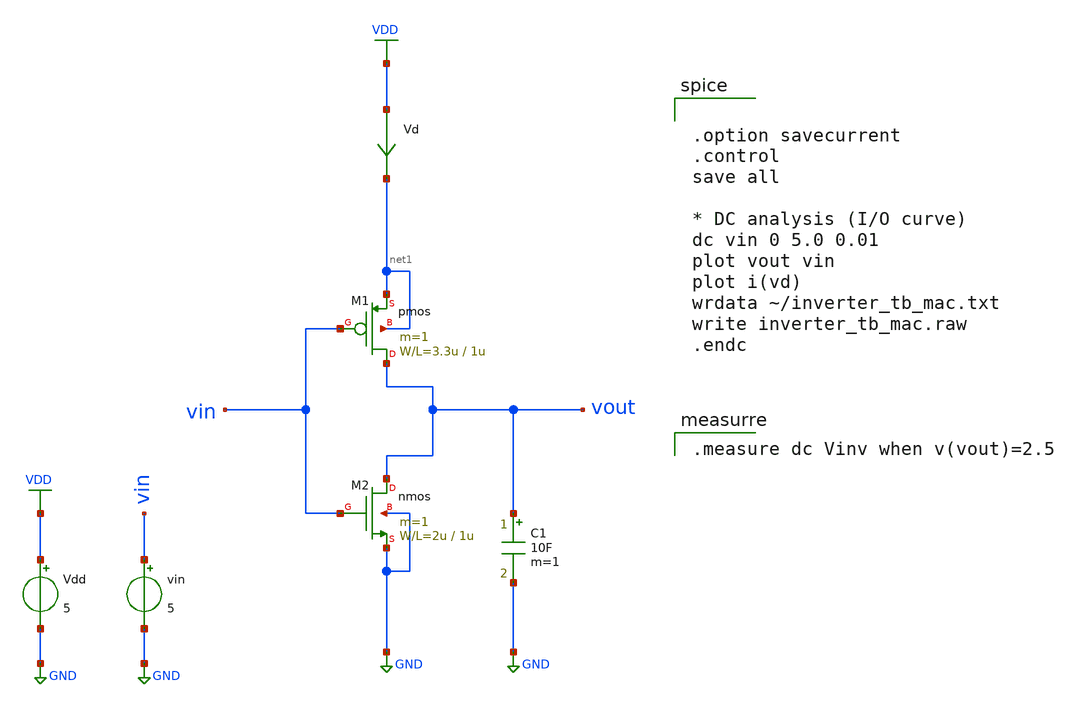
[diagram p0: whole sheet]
** sch_path: member_project/YutakaKOTANI/tb_inv_yutaka.sch
**.subckt tb_inv_yutaka
M1 vout vin net1 net1 pmos L=1u W=3.3u m=1
M2 vout vin GND GND nmos L=1u W=2u m=1
Vd VDD net1 0
.save i(vd)
C1 vout GND 10F m=1
Vdd VDD GND 5
vin vin GND 5
**** begin user architecture code
 .include $::LIB/mos.lib
.include $::LIB/passive.lib
.include $::LIB/diode.lib


.option savecurrent
.control
save all

* DC analysis (I/O curve)
dc vin 0 5.0 0.01
plot vout vin
plot i(vd)
wrdata ~/inverter_tb_mac.txt
write inverter_tb_mac.raw
.endc



.measure dc Vinv when v(vout)=2.5

**** end user architecture code
**.ends
.GLOBAL VDD
.GLOBAL GND
.end
